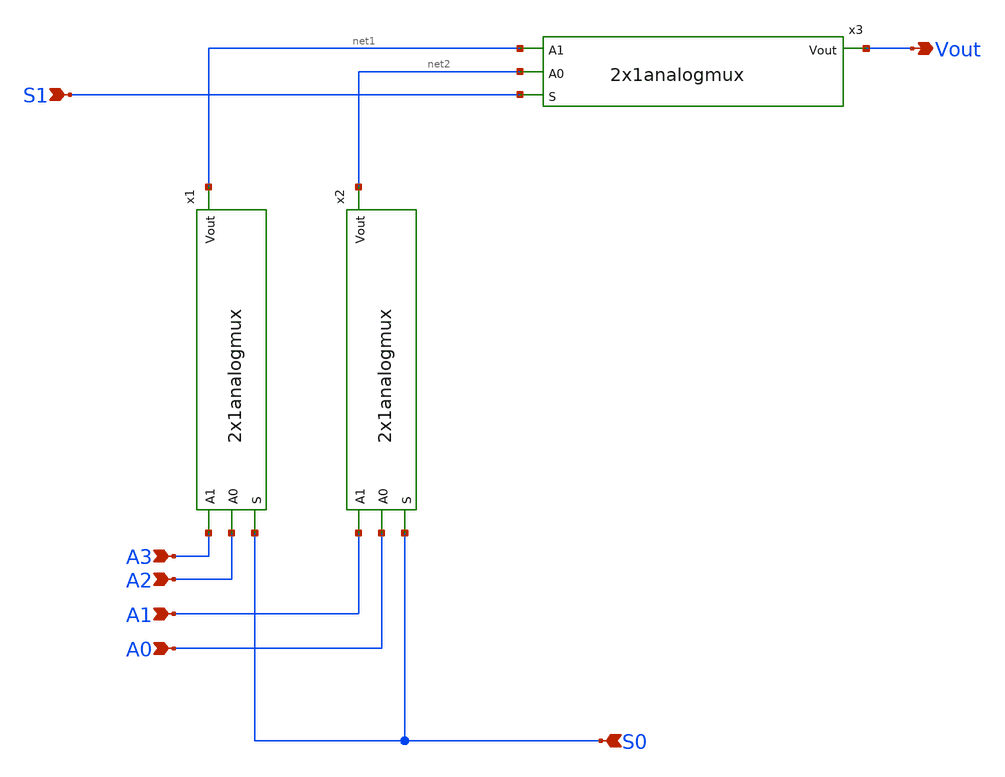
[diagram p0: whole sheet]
** sch_path: 4x1analogmux.sch
* 2x1analogmux.sch:
* Copyright 2021 Stefan Frederik Schippers
* Licensed under the Apache License, Version 2.0 (the "License");
**.subckt 4x1analogmux A3 A2 A1 A0 S1 S0 Vout
*.ipin A3
*.ipin A2
*.ipin A1
*.ipin A0
*.ipin S1
*.ipin S0
*.opin Vout
x2 net2 A1 A0 S0 2x1analogmux
x3 Vout net1 net2 S1 2x1analogmux
x1 net1 A3 A2 S0 2x1analogmux
**.ends

* expanding   symbol:  2x1analogmux.sym # of pins=4
** sym_path: 2x1analogmux.sym
** sch_path: 2x1analogmux.sch
.subckt 2x1analogmux Vout A1 A0 S
*.ipin S
*.opin Vout
*.ipin A1
*.ipin A0
x1 net1 A1 Vout S dacpassgate
x2 S A0 Vout net1 dacpassgate
x4 net1 S VDD GND not W_N=1 L_N=0.15 W_P=2 L_P=0.15 m=10
.ends


* expanding   symbol:  dacpassgate.sym # of pins=4
** sym_path: dacpassgate.sym
** sch_path: dacpassgate.sch
.subckt dacpassgate GP A Z GN
*.iopin A
*.iopin Z
*.ipin GP
*.ipin GN
XM1 net1 GN A GND sky130_fd_pr__nfet_01v8 L=0.5 W=1 nf=1 ad='int((nf+1)/2) * W/nf * 0.29' as='int((nf+2)/2) * W/nf * 0.29'
+ pd='2*int((nf+1)/2) * (W/nf + 0.29)' ps='2*int((nf+2)/2) * (W/nf + 0.29)' nrd='0.29 / W' nrs='0.29 / W'
+ sa=0 sb=0 sd=0 mult=10 m=10
XM2 net2 GP A VDD sky130_fd_pr__pfet_01v8 L=0.5 W=2 nf=1 ad='int((nf+1)/2) * W/nf * 0.29' as='int((nf+2)/2) * W/nf * 0.29'
+ pd='2*int((nf+1)/2) * (W/nf + 0.29)' ps='2*int((nf+2)/2) * (W/nf + 0.29)' nrd='0.29 / W' nrs='0.29 / W'
+ sa=0 sb=0 sd=0 mult=10 m=10
vidp net2 Z 0
vidn Z net1 0
.ends


* expanding   symbol:  sky130_tests/not.sym # of pins=2
** sym_path: sky130_tests/not.sym
** sch_path: sky130_tests/not.sch
.subckt not y a VCCPIN VSSPIN     W_N=1 L_N=0.15 W_P=2 L_P=0.15
*.opin y
*.ipin a
XM1 DN a VSSPIN VSSPIN sky130_fd_pr__nfet_01v8 L=L_N W=W_N nf=1 ad='int((1 + 1)/2) * W_N / 1 * 0.29'
+ as='int((1 + 2)/2) * W_N / 1 * 0.29' pd='2*int((1 + 1)/2) * (W_N / 1 + 0.29)' ps='2*int((1 + 2)/2) * (W_N / 1 + 0.29)'
+ nrd='0.29 / W_N ' nrs='0.29 / W_N ' sa=0 sb=0 sd=0 mult=1 m=1
XM2 DP a VCCPIN VCCPIN sky130_fd_pr__pfet_01v8 L=L_P W=W_P nf=1 ad='int((nf+1)/2) * W/nf * 0.29' as='int((nf+2)/2) * W/nf * 0.29'
+ pd='2*int((nf+1)/2) * (W/nf + 0.29)' ps='2*int((nf+2)/2) * (W/nf + 0.29)' nrd='0.29 / W' nrs='0.29 / W'
+ sa=0 sb=0 sd=0 mult=1 m=1
Vmeas DP y 0
.save i(vmeas)
Vmeas1 y DN 0
.save i(vmeas1)
.save v(dp)
.save v(dn)
.ends

.end
